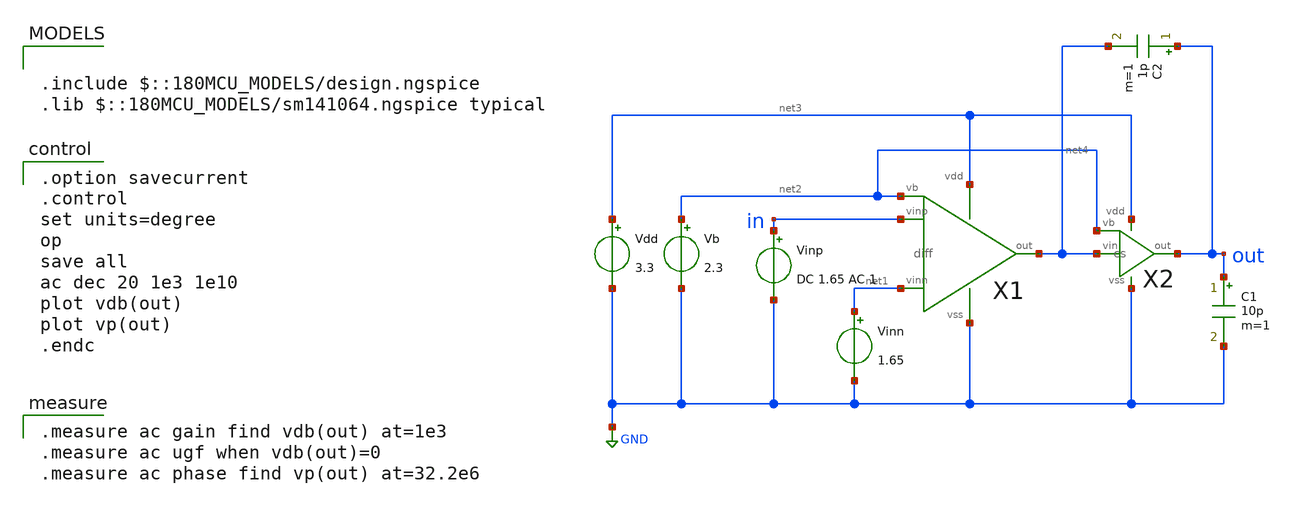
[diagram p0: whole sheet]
** sch_path: opamp/2stage_cc_ac.sch
**.subckt 2stage_cc_ac
Vdd net3 GND 3.3
Vb net2 GND 2.3
Vinn net1 GND 1.65
Vinp in GND DC 1.65 AC 1
X1 in net1 net4 net3 GND net2 diff
X2 net4 net2 out net3 GND cs
C1 out GND 10p m=1
C2 out net4 1p m=1
**** begin user architecture code

.include $::180MCU_MODELS/design.ngspice
.lib $::180MCU_MODELS/sm141064.ngspice typical


.option savecurrent
.control
set units=degree
op
save all
ac dec 20 1e3 1e10
plot vdb(out)
plot vp(out)
.endc


.measure ac gain find vdb(out) at=1e3
.measure ac ugf when vdb(out)=0
.measure ac phase find vp(out) at=32.2e6

**** end user architecture code
**.ends
.GLOBAL GND
.end
